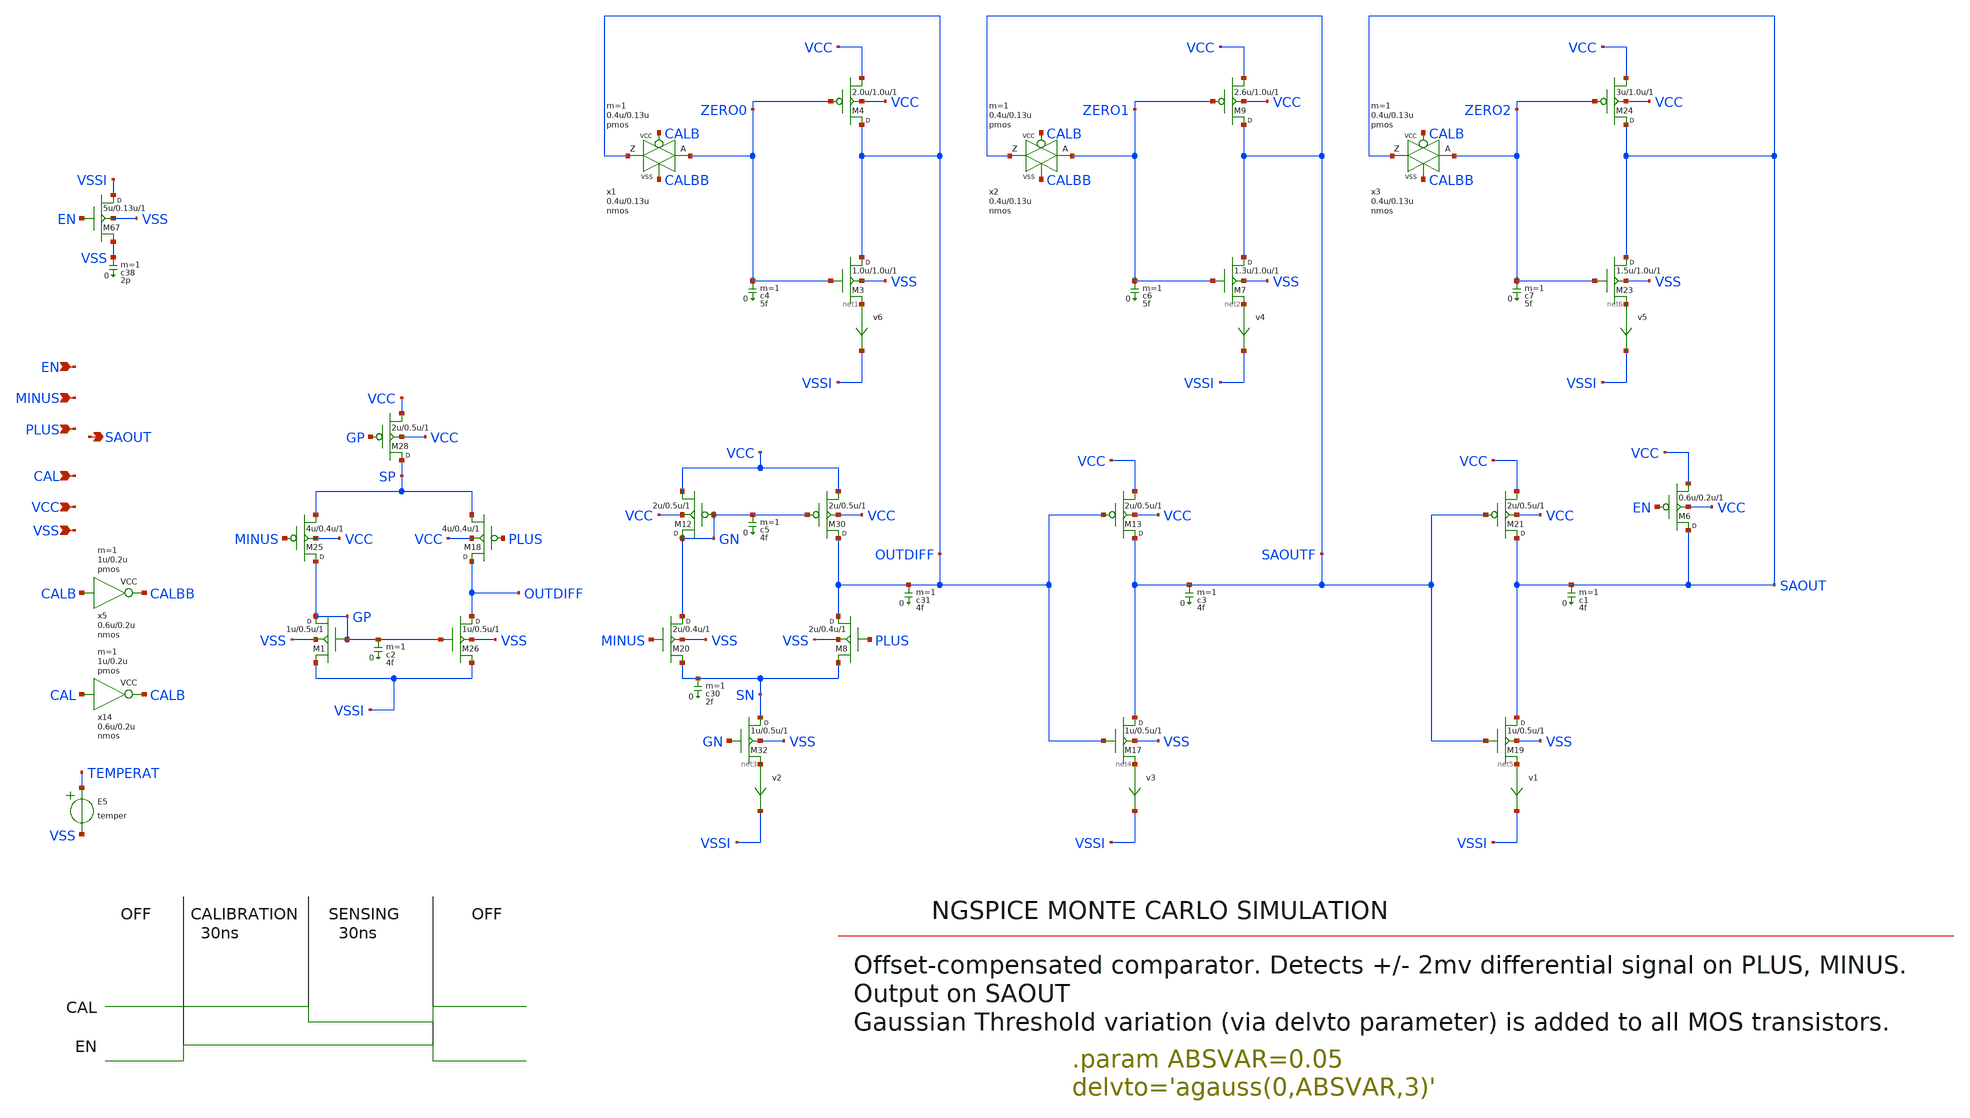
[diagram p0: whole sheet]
** sch_path: xschem_library/ngspice/autozero_comp.sch
**.subckt autozero_comp CAL PLUS MINUS EN VSS VCC SAOUT
*.ipin CAL
*.ipin PLUS
*.ipin MINUS
*.ipin EN
*.ipin VSS
*.ipin VCC
*.opin SAOUT
E5 TEMPERAT VSS VOL=' temper '
MAx14 CALB CAL VCC VCC pmos w=1u l=0.2u m=1
MBx14 CALB CAL VSS VSS nmos w=0.6u l=0.2u m=1
MAx5 CALBB CALB VCC VCC pmos w=1u l=0.2u m=1
MBx5 CALBB CALB VSS VSS nmos w=0.6u l=0.2u m=1
M67 VSSI EN VSS VSS nmos w=5u l=0.13u delvto='agauss(0,ABSVAR,3)' m=1
c38 VSS 0 2p m=1
MAx1 OUTDIFF CALB ZERO0 VCC pmos w=0.4u l=0.13u delvto='agauss(0,ABSVAR,3)' m=1
MBx1 OUTDIFF CALBB ZERO0 VSS nmos w=0.4u l=0.13u delvto='agauss(0,ABSVAR,3)' m=1
M3 OUTDIFF ZERO0 net1 VSS nmos w=1.0u l=1.0u delvto='agauss(0,ABSVAR,3)' m=1
M4 OUTDIFF ZERO0 VCC VCC pmos w=2.0u l=1.0u delvto='agauss(0,ABSVAR,3)' m=1
MAx2 SAOUTF CALB ZERO1 VCC pmos w=0.4u l=0.13u delvto='agauss(0,ABSVAR,3)' m=1
MBx2 SAOUTF CALBB ZERO1 VSS nmos w=0.4u l=0.13u delvto='agauss(0,ABSVAR,3)' m=1
M7 SAOUTF ZERO1 net2 VSS nmos w=1.3u l=1.0u delvto='agauss(0,ABSVAR,3)' m=1
M9 SAOUTF ZERO1 VCC VCC pmos w=2.6u l=1.0u delvto='agauss(0,ABSVAR,3)' m=1
M20 GN MINUS SN VSS nmos w=2u l=0.4u delvto='agauss(0,ABSVAR,3)' m=1
M8 OUTDIFF PLUS SN VSS nmos w=2u l=0.4u delvto='agauss(0,ABSVAR,3)' m=1
M30 OUTDIFF GN VCC VCC pmos w=2u l=0.5u delvto='agauss(0,ABSVAR,3)' m=1
M12 GN GN VCC VCC pmos w=2u l=0.5u delvto='agauss(0,ABSVAR,3)' m=1
M32 SN GN net3 VSS nmos w=1u l=0.5u delvto='agauss(0,ABSVAR,3)' m=1
M17 SAOUTF OUTDIFF net4 VSS nmos w=1u l=0.5u delvto='agauss(0,ABSVAR,3)' m=1
M13 SAOUTF OUTDIFF VCC VCC pmos w=2u l=0.5u delvto='agauss(0,ABSVAR,3)' m=1
c3 SAOUTF 0 4f m=1
c5 GN 0 4f m=1
c30 SN 0 2f m=1
c31 OUTDIFF 0 4f m=1
v2 net3 VSSI 0
.save i(v2)
v3 net4 VSSI 0
.save i(v3)
v4 net2 VSSI 0
.save i(v4)
v6 net1 VSSI 0
.save i(v6)
M19 SAOUT SAOUTF net5 VSS nmos w=1u l=0.5u delvto='agauss(0,ABSVAR,3)' m=1
M21 SAOUT SAOUTF VCC VCC pmos w=2u l=0.5u delvto='agauss(0,ABSVAR,3)' m=1
c1 SAOUT 0 4f m=1
v1 net5 VSSI 0
.save i(v1)
MAx3 SAOUT CALB ZERO2 VCC pmos w=0.4u l=0.13u delvto='agauss(0,ABSVAR,3)' m=1
MBx3 SAOUT CALBB ZERO2 VSS nmos w=0.4u l=0.13u delvto='agauss(0,ABSVAR,3)' m=1
M23 SAOUT ZERO2 net6 VSS nmos w=1.5u l=1.0u delvto='agauss(0,ABSVAR,3)' m=1
M24 SAOUT ZERO2 VCC VCC pmos w=3u l=1.0u delvto='agauss(0,ABSVAR,3)' m=1
v5 net6 VSSI 0
.save i(v5)
M6 SAOUT EN VCC VCC pmos w=0.6u l=0.2u delvto='agauss(0,ABSVAR,3)' m=1
M18 OUTDIFF PLUS SP VCC pmos w=4u l=0.4u delvto='agauss(0,ABSVAR,3)' m=1
M25 GP MINUS SP VCC pmos w=4u l=0.4u delvto='agauss(0,ABSVAR,3)' m=1
M28 SP GP VCC VCC pmos w=2u l=0.5u delvto='agauss(0,ABSVAR,3)' m=1
M26 OUTDIFF GP VSSI VSS nmos w=1u l=0.5u delvto='agauss(0,ABSVAR,3)' m=1
M1 GP GP VSSI VSS nmos w=1u l=0.5u delvto='agauss(0,ABSVAR,3)' m=1
c2 GP 0 4f m=1
c4 ZERO0 0 5f m=1
c6 ZERO1 0 5f m=1
c7 ZERO2 0 5f m=1
**.ends
**** begin user architecture code

* .option SCALE=1e-6
.option method=gear seed=12
.param VCC=0.9
.param VDL='VCC/2+0.2'
.param ABSVAR=0.05
.temp 25

** to generate following file:
** copy .../share/doc/xschem/ngspice/stimuli.autozero_comp to simulation directory
** then do 'Simulation->Utile Stimuli Editor (GUI)' and press 'Translate'
.include "stimuli_autozero_comp.cir"

** download models from here:
** http://ptm.asu.edu/modelcard/2006/130nm_bulk.pm
** and save to 'models_autozero_comp.txt' in simulation directory
.include "models_autozero_comp.txt"


* .tran 0.1n 900n uic

.control
  let run=1

  dowhile run <= 10
    if run > 1
      reset
      set appendwrite
    end
    save saout cal i(vvcc) en plus minus saoutf outdiff
    tran 0.1n 900n uic
    write autozero_comp.raw
    let run = run + 1
  end
.endc


**** end user architecture code
.end
